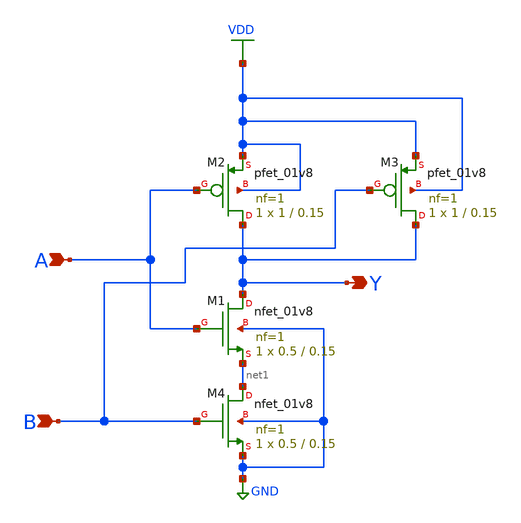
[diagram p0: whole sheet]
** sch_path: library/xschem/nand.sch
**.subckt nand A Y B
*.ipin A
*.opin Y
*.ipin B
XM1 Y A net1 GND sky130_fd_pr__nfet_01v8 L=0.15 W=0.5 nf=1 ad='int((nf+1)/2) * W/nf * 0.29' as='int((nf+2)/2) * W/nf * 0.29'
+ pd='2*int((nf+1)/2) * (W/nf + 0.29)' ps='2*int((nf+2)/2) * (W/nf + 0.29)' nrd='0.29 / W' nrs='0.29 / W'
+ sa=0 sb=0 sd=0 mult=1 m=1
XM2 Y A VDD VDD sky130_fd_pr__pfet_01v8 L=0.15 W=1 nf=1 ad='int((nf+1)/2) * W/nf * 0.29' as='int((nf+2)/2) * W/nf * 0.29'
+ pd='2*int((nf+1)/2) * (W/nf + 0.29)' ps='2*int((nf+2)/2) * (W/nf + 0.29)' nrd='0.29 / W' nrs='0.29 / W'
+ sa=0 sb=0 sd=0 mult=1 m=1
XM3 Y B VDD VDD sky130_fd_pr__pfet_01v8 L=0.15 W=1 nf=1 ad='int((nf+1)/2) * W/nf * 0.29' as='int((nf+2)/2) * W/nf * 0.29'
+ pd='2*int((nf+1)/2) * (W/nf + 0.29)' ps='2*int((nf+2)/2) * (W/nf + 0.29)' nrd='0.29 / W' nrs='0.29 / W'
+ sa=0 sb=0 sd=0 mult=1 m=1
XM4 net1 B GND GND sky130_fd_pr__nfet_01v8 L=0.15 W=0.5 nf=1 ad='int((nf+1)/2) * W/nf * 0.29' as='int((nf+2)/2) * W/nf * 0.29'
+ pd='2*int((nf+1)/2) * (W/nf + 0.29)' ps='2*int((nf+2)/2) * (W/nf + 0.29)' nrd='0.29 / W' nrs='0.29 / W'
+ sa=0 sb=0 sd=0 mult=1 m=1
**.ends
.GLOBAL VDD
.GLOBAL GND
.end
